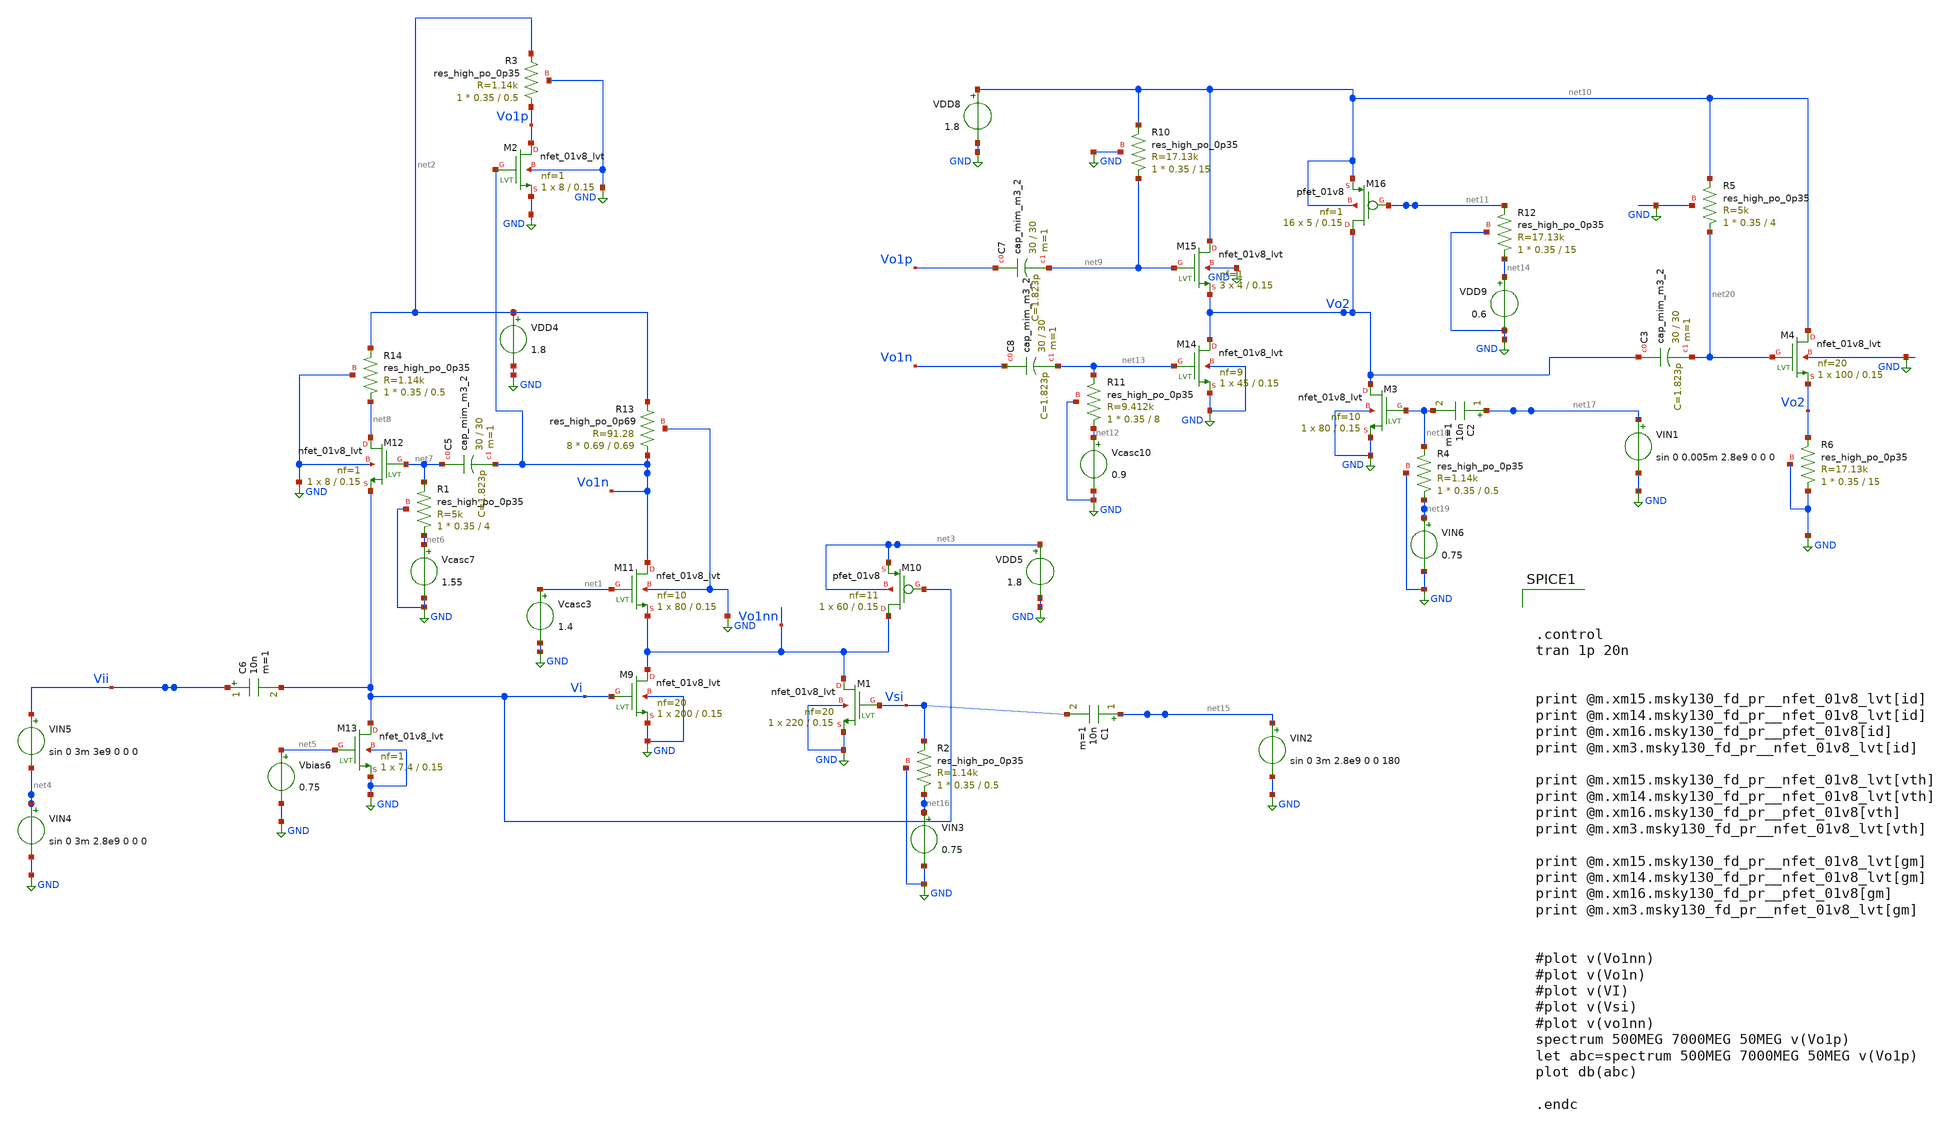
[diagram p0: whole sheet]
** sch_path: xschem/xschem4_sic_final/CompleteAMP6with50ohms1.sch
**.subckt CompleteAMP6with50ohms1
Vcasc3 net1 GND 1.4
VDD4 net2 GND 1.8
VDD5 net3 GND 1.8
Vbias6 net5 GND 0.75
Vcasc7 net6 GND 1.55
XR1 net6 net7 GND sky130_fd_pr__res_high_po_0p35 L=4 mult=1 m=1
XC5 net7 Vo1n sky130_fd_pr__cap_mim_m3_2 W=30 L=30 MF=1 m=1
C6 Vii Vi 10n m=1
XM9 Vo1nn Vi GND GND sky130_fd_pr__nfet_01v8_lvt L=0.15 W=200 nf=20 ad='int((nf+1)/2) * W/nf * 0.29'
+ as='int((nf+2)/2) * W/nf * 0.29' pd='2*int((nf+1)/2) * (W/nf + 0.29)' ps='2*int((nf+2)/2) * (W/nf + 0.29)'
+ nrd='0.29 / W' nrs='0.29 / W' sa=0 sb=0 sd=0 mult=1 m=1
XM10 Vo1nn Vi net3 net3 sky130_fd_pr__pfet_01v8 L=0.15 W=60 nf=11 ad='int((nf+1)/2) * W/nf * 0.29' as='int((nf+2)/2) * W/nf * 0.29'
+ pd='2*int((nf+1)/2) * (W/nf + 0.29)' ps='2*int((nf+2)/2) * (W/nf + 0.29)' nrd='0.29 / W' nrs='0.29 / W'
+ sa=0 sb=0 sd=0 mult=1 m=1
XM11 Vo1n net1 Vo1nn GND sky130_fd_pr__nfet_01v8_lvt L=0.15 W=80 nf=10 ad='int((nf+1)/2) * W/nf * 0.29'
+ as='int((nf+2)/2) * W/nf * 0.29' pd='2*int((nf+1)/2) * (W/nf + 0.29)' ps='2*int((nf+2)/2) * (W/nf + 0.29)'
+ nrd='0.29 / W' nrs='0.29 / W' sa=0 sb=0 sd=0 mult=1 m=1
XM12 net8 net7 Vi GND sky130_fd_pr__nfet_01v8_lvt L=0.15 W=8 nf=1 ad='int((nf+1)/2) * W/nf * 0.29' as='int((nf+2)/2) * W/nf * 0.29'
+ pd='2*int((nf+1)/2) * (W/nf + 0.29)' ps='2*int((nf+2)/2) * (W/nf + 0.29)' nrd='0.29 / W' nrs='0.29 / W'
+ sa=0 sb=0 sd=0 mult=1 m=1
XM13 Vi net5 GND GND sky130_fd_pr__nfet_01v8_lvt L=0.15 W=7.4 nf=1 ad='int((nf+1)/2) * W/nf * 0.29' as='int((nf+2)/2) * W/nf * 0.29'
+ pd='2*int((nf+1)/2) * (W/nf + 0.29)' ps='2*int((nf+2)/2) * (W/nf + 0.29)' nrd='0.29 / W' nrs='0.29 / W'
+ sa=0 sb=0 sd=0 mult=1 m=1
XM14 Vo2 net13 GND GND sky130_fd_pr__nfet_01v8_lvt L=0.15 W=45 nf=9 ad='int((nf+1)/2) * W/nf * 0.29'
+ as='int((nf+2)/2) * W/nf * 0.29' pd='2*int((nf+1)/2) * (W/nf + 0.29)' ps='2*int((nf+2)/2) * (W/nf + 0.29)'
+ nrd='0.29 / W' nrs='0.29 / W' sa=0 sb=0 sd=0 mult=1 m=1
XM15 net10 net9 Vo2 GND sky130_fd_pr__nfet_01v8_lvt L=0.15 W=4 nf=1 ad='int((nf+1)/2) * W/nf * 0.29'
+ as='int((nf+2)/2) * W/nf * 0.29' pd='2*int((nf+1)/2) * (W/nf + 0.29)' ps='2*int((nf+2)/2) * (W/nf + 0.29)'
+ nrd='0.29 / W' nrs='0.29 / W' sa=0 sb=0 sd=0 mult=3 m=3
XR10 net9 net10 GND sky130_fd_pr__res_high_po_0p35 L=15 mult=1 m=1
XM16 Vo2 net11 net10 net10 sky130_fd_pr__pfet_01v8 L=0.15 W=5 nf=1 ad='int((nf+1)/2) * W/nf * 0.29' as='int((nf+2)/2) * W/nf * 0.29'
+ pd='2*int((nf+1)/2) * (W/nf + 0.29)' ps='2*int((nf+2)/2) * (W/nf + 0.29)' nrd='0.29 / W' nrs='0.29 / W'
+ sa=0 sb=0 sd=0 mult=16 m=16
VDD8 net10 GND 1.8
VDD9 net14 GND 0.6
XC7 Vo1p net9 sky130_fd_pr__cap_mim_m3_2 W=30 L=30 MF=1 m=1
Vcasc10 net12 GND 0.9
XR11 net12 net13 GND sky130_fd_pr__res_high_po_0p35 L=8 mult=1 m=1
XC8 Vo1n net13 sky130_fd_pr__cap_mim_m3_2 W=30 L=30 MF=1 m=1
XR12 net14 net11 GND sky130_fd_pr__res_high_po_0p35 L=15 mult=1 m=1
XR14 net8 net2 GND sky130_fd_pr__res_high_po_0p35 L=0.5 mult=1 m=1
XM1 Vo1nn Vsi GND GND sky130_fd_pr__nfet_01v8_lvt L=0.15 W=220 nf=20 ad='int((nf+1)/2) * W/nf * 0.29'
+ as='int((nf+2)/2) * W/nf * 0.29' pd='2*int((nf+1)/2) * (W/nf + 0.29)' ps='2*int((nf+2)/2) * (W/nf + 0.29)'
+ nrd='0.29 / W' nrs='0.29 / W' sa=0 sb=0 sd=0 mult=1 m=1
VIN2 net15 GND sin 0 3m 2.8e9 0 0 180
C1 net15 Vsi 10n m=1
VIN3 net16 GND 0.75
VIN4 net4 GND sin 0 3m 2.8e9 0 0 0
XR13 Vo1n net2 GND sky130_fd_pr__res_high_po_0p69 L=0.69 mult=8 m=8
VIN5 Vii net4 sin 0 3m 3e9 0 0 0
XR2 net16 Vsi GND sky130_fd_pr__res_high_po_0p35 L=0.5 mult=1 m=1
XM2 Vo1p Vo1n GND GND sky130_fd_pr__nfet_01v8_lvt L=0.15 W=8 nf=1 ad='int((nf+1)/2) * W/nf * 0.29' as='int((nf+2)/2) * W/nf * 0.29'
+ pd='2*int((nf+1)/2) * (W/nf + 0.29)' ps='2*int((nf+2)/2) * (W/nf + 0.29)' nrd='0.29 / W' nrs='0.29 / W'
+ sa=0 sb=0 sd=0 mult=1 m=1
XR3 Vo1p net2 GND sky130_fd_pr__res_high_po_0p35 L=0.5 mult=1 m=1
XM3 Vo2 net18 GND GND sky130_fd_pr__nfet_01v8_lvt L=0.15 W=80 nf=10 ad='int((nf+1)/2) * W/nf * 0.29'
+ as='int((nf+2)/2) * W/nf * 0.29' pd='2*int((nf+1)/2) * (W/nf + 0.29)' ps='2*int((nf+2)/2) * (W/nf + 0.29)'
+ nrd='0.29 / W' nrs='0.29 / W' sa=0 sb=0 sd=0 mult=1 m=1
VIN1 net17 GND sin 0 0.005m 2.8e9 0 0 0
C2 net17 net18 10n m=1
VIN6 net19 GND 0.75
XR4 net19 net18 GND sky130_fd_pr__res_high_po_0p35 L=0.5 mult=1 m=1
XM4 net10 net20 Vo2 GND sky130_fd_pr__nfet_01v8_lvt L=0.15 W=100 nf=20 ad='int((nf+1)/2) * W/nf * 0.29'
+ as='int((nf+2)/2) * W/nf * 0.29' pd='2*int((nf+1)/2) * (W/nf + 0.29)' ps='2*int((nf+2)/2) * (W/nf + 0.29)'
+ nrd='0.29 / W' nrs='0.29 / W' sa=0 sb=0 sd=0 mult=1 m=1
XR5 net20 net10 GND sky130_fd_pr__res_high_po_0p35 L=4 mult=1 m=1
XR6 GND Vo2 GND sky130_fd_pr__res_high_po_0p35 L=15 mult=1 m=1
XC3 Vo2 net20 sky130_fd_pr__cap_mim_m3_2 W=30 L=30 MF=1 m=1
**** begin user architecture code

.lib $::SKYWATER_MODELS/sky130.lib.spice tt




.control
tran 1p 20n


print @m.xm15.msky130_fd_pr__nfet_01v8_lvt[id]
print @m.xm14.msky130_fd_pr__nfet_01v8_lvt[id]
print @m.xm16.msky130_fd_pr__pfet_01v8[id]
print @m.xm3.msky130_fd_pr__nfet_01v8_lvt[id]

print @m.xm15.msky130_fd_pr__nfet_01v8_lvt[vth]
print @m.xm14.msky130_fd_pr__nfet_01v8_lvt[vth]
print @m.xm16.msky130_fd_pr__pfet_01v8[vth]
print @m.xm3.msky130_fd_pr__nfet_01v8_lvt[vth]

print @m.xm15.msky130_fd_pr__nfet_01v8_lvt[gm]
print @m.xm14.msky130_fd_pr__nfet_01v8_lvt[gm]
print @m.xm16.msky130_fd_pr__pfet_01v8[gm]
print @m.xm3.msky130_fd_pr__nfet_01v8_lvt[gm]


#plot v(Vo1nn)
#plot v(Vo1n)
#plot v(VI)
#plot v(Vsi)
#plot v(vo1nn)
spectrum 500MEG 7000MEG 50MEG v(Vo1p)
let abc=spectrum 500MEG 7000MEG 50MEG v(Vo1p)
plot db(abc)

.endc


**** end user architecture code
**.ends
.GLOBAL GND
.end
